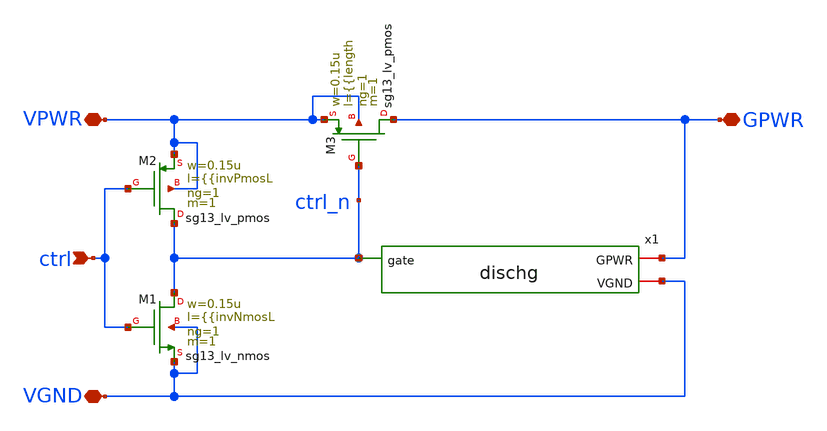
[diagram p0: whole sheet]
** sch_path: ihp-sg13cmos5l/libs.tech/generators/hm_pg/hm_pg_lv/xschem/hm_pg_lv.sch
**.subckt hm_pg_lv ctrl VPWR VGND GPWR
*.ipin ctrl
*.iopin VPWR
*.iopin VGND
*.iopin GPWR
XM1 ctrl_n ctrl VGND VGND sg13_lv_nmos w=0.15u l={{invNmosL ng=1 m=1 mm_ok=1
XM2 ctrl_n ctrl VPWR VPWR sg13_lv_pmos w=0.15u l={{invPmosL ng=1 m=1 mm_ok=1
XM3 GPWR ctrl_n VPWR VPWR sg13_lv_pmos w=0.15u l={{length ng=1 m=1 mm_ok=1
x1 VGND GPWR ctrl_n dischg
**.ends

* expanding   symbol:  hm_analog/dischg.sym # of pins=3
** sym_path: ihp-sg13cmos5l/libs.tech/xschem/hm_analog/dischg.sym
** sch_path: ihp-sg13cmos5l/libs.tech/xschem/hm_analog/dischg.sch
.subckt dischg VGND GPWR gate
*.iopin GPWR
*.iopin VGND
*.ipin gate
XM1 GPWR gate net2 VGND sg13_lv_nmos w=4u l=0.65u ng=1 m=1 mm_ok=1
XM2 net2 gate net3 VGND sg13_lv_nmos w=4u l=0.65u ng=1 m=1 mm_ok=1
XM3 net3 gate net4 VGND sg13_lv_nmos w=4u l=0.65u ng=1 m=1 mm_ok=1
XM4 net4 gate net1 VGND sg13_lv_nmos w=4u l=0.65u ng=1 m=1 mm_ok=1
XM5 net1 gate net7 VGND sg13_lv_nmos w=4u l=0.65u ng=1 m=1 mm_ok=1
XM6 net7 gate net6 VGND sg13_lv_nmos w=4u l=0.65u ng=1 m=1 mm_ok=1
XM7 net6 gate net5 VGND sg13_lv_nmos w=4u l=0.65u ng=1 m=1 mm_ok=1
XM8 net5 gate VGND VGND sg13_lv_nmos w=4u l=0.65u ng=1 m=1 mm_ok=1
XM9 GPWR gate net9 VGND sg13_lv_nmos w=4u l=0.65u ng=1 m=1 mm_ok=1
XM10 net9 gate net10 VGND sg13_lv_nmos w=4u l=0.65u ng=1 m=1 mm_ok=1
XM11 net10 gate net11 VGND sg13_lv_nmos w=4u l=0.65u ng=1 m=1 mm_ok=1
XM12 net11 gate net8 VGND sg13_lv_nmos w=4u l=0.65u ng=1 m=1 mm_ok=1
XM13 net8 gate net14 VGND sg13_lv_nmos w=4u l=0.65u ng=1 m=1 mm_ok=1
XM14 net14 gate net13 VGND sg13_lv_nmos w=4u l=0.65u ng=1 m=1 mm_ok=1
XM15 net13 gate net12 VGND sg13_lv_nmos w=4u l=0.65u ng=1 m=1 mm_ok=1
XM16 net12 gate VGND VGND sg13_lv_nmos w=4u l=0.65u ng=1 m=1 mm_ok=1
.ends

.end
